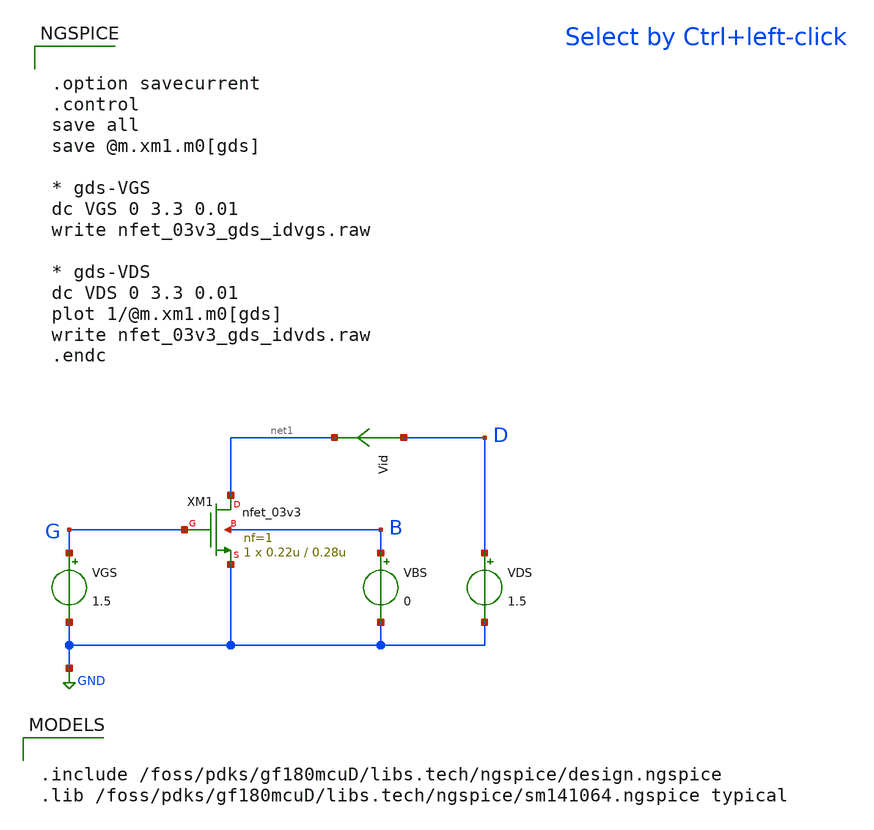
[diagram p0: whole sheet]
** sch_path: mosfet_gf180/nfet_03v3_gds.sch
**.subckt nfet_03v3_gds
XM1 net1 G GND B nfet_03v3 L=0.28u W=0.22u nf=1 ad='int((nf+1)/2) * W/nf * 0.18u' as='int((nf+2)/2) * W/nf * 0.18u'
+ pd='2*int((nf+1)/2) * (W/nf + 0.18u)' ps='2*int((nf+2)/2) * (W/nf + 0.18u)' nrd='0.18u / W' nrs='0.18u / W'
+ sa=0 sb=0 sd=0 m=1
VBS B GND 0
VGS G GND 1.5
VDS D GND 1.5
Vid D net1 0
.save i(vid)
**** begin user architecture code

.include /foss/pdks/gf180mcuD/libs.tech/ngspice/design.ngspice
.lib /foss/pdks/gf180mcuD/libs.tech/ngspice/sm141064.ngspice typical



.option savecurrent
.control
save all
save @m.xm1.m0[gds]

* gds-VGS
dc VGS 0 3.3 0.01
write nfet_03v3_gds_idvgs.raw

* gds-VDS
dc VDS 0 3.3 0.01
plot 1/@m.xm1.m0[gds]
write nfet_03v3_gds_idvds.raw
.endc


**** end user architecture code
**.ends
.GLOBAL GND
.end
